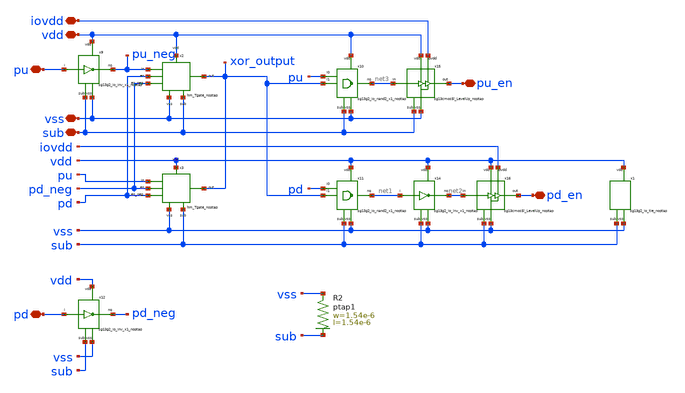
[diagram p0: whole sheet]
** sch_path: ihp-sg13cmos5l/libs.tech/xschem/hm_stdcells/hm_PUPD_decoder.sch
**.subckt hm_PUPD_decoder pu pd iovdd vdd vss sub pu_en pd_en
*.iopin pu
*.iopin pd
*.iopin iovdd
*.iopin vdd
*.iopin vss
*.iopin sub
*.iopin pu_en
*.iopin pd_en
x9 vss pu pu_neg vdd sub sg13g2_io_inv_x1_noptap
x10 vss pu net3 vdd sub xor_output sg13g2_io_nand2_x1_noptap
x11 vss pd net1 vdd sub xor_output sg13g2_io_nand2_x1_noptap
x12 vss pd pd_neg vdd sub sg13g2_io_inv_x1_noptap
x14 vss net1 net2 vdd sub sg13g2_io_inv_x1_noptap
x15 iovdd vss net3 pu_en vdd sub sg13cmos5l_LevelUp_noptap
x16 iovdd vss net2 pd_en vdd sub sg13cmos5l_LevelUp_noptap
x1 vss vdd sub sg13g2_io_tie_noptap
XR2 vss sub ptap1 R=114.9 w=1.54e-6 l=1.54e-6
x2 pd sub pu_neg xor_output vdd pd_neg vss hm_Tgate_noptap
x3 pd_neg sub pu xor_output vdd pd vss hm_Tgate_noptap
**.ends
.end
